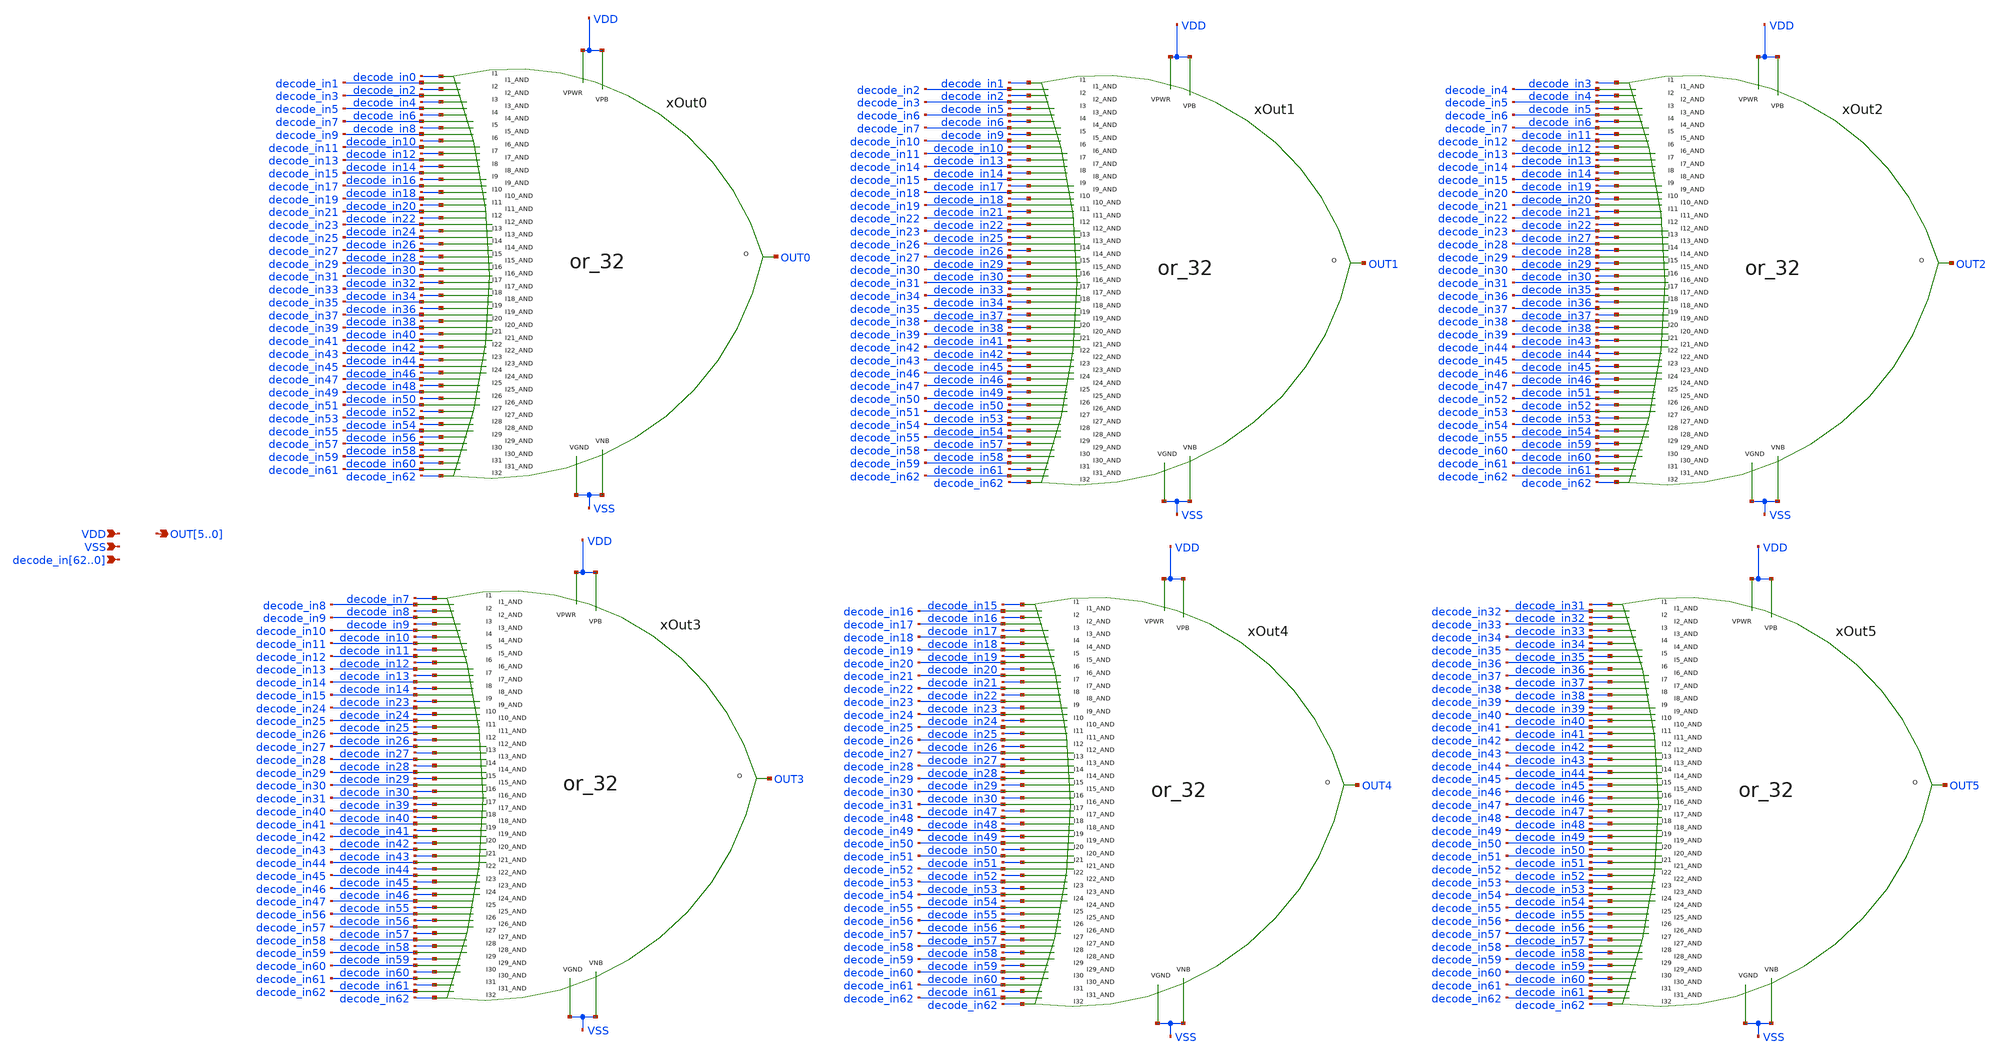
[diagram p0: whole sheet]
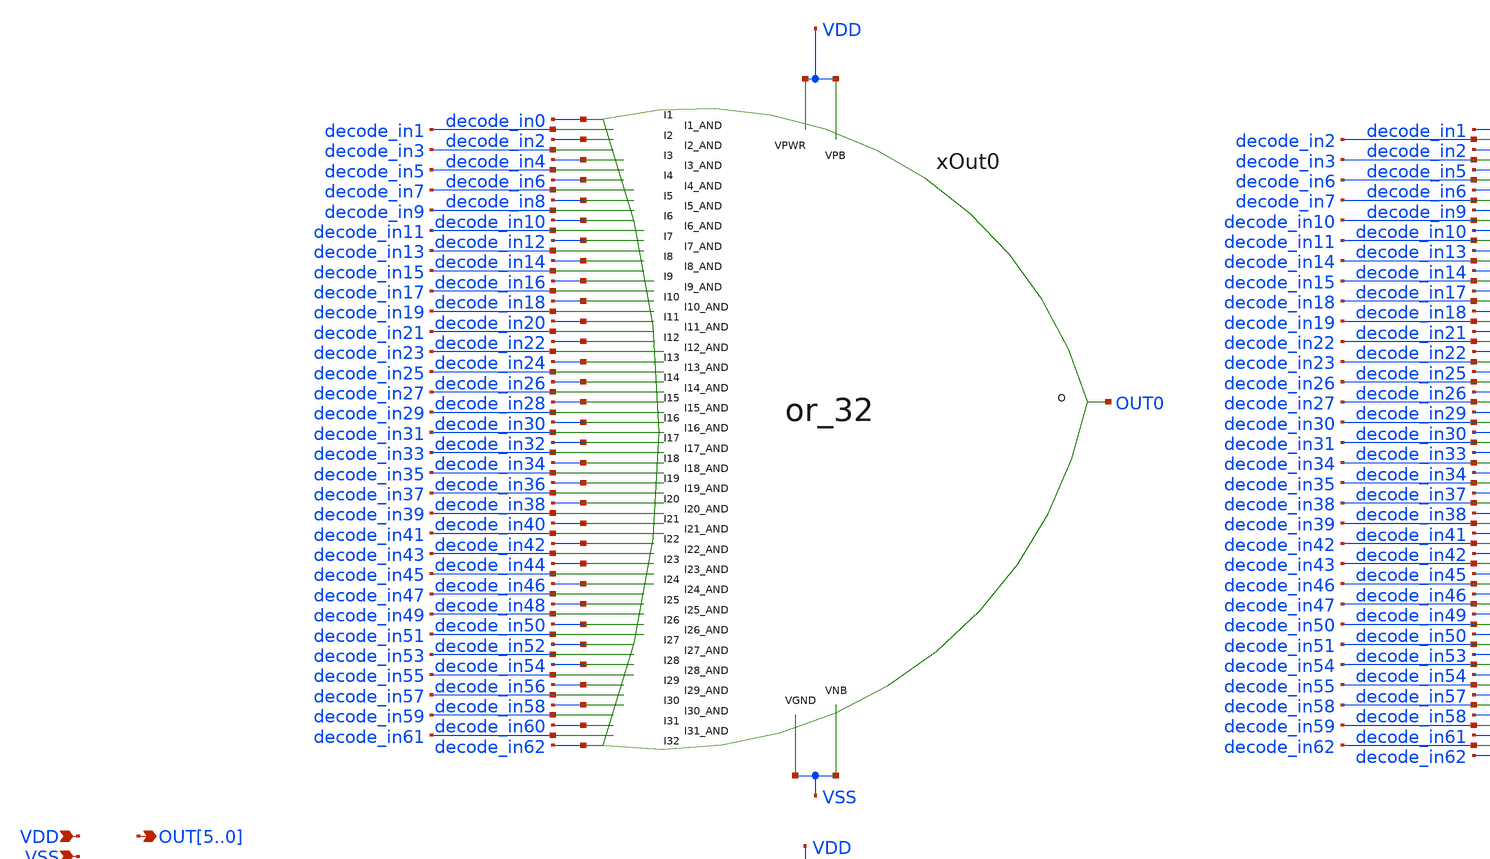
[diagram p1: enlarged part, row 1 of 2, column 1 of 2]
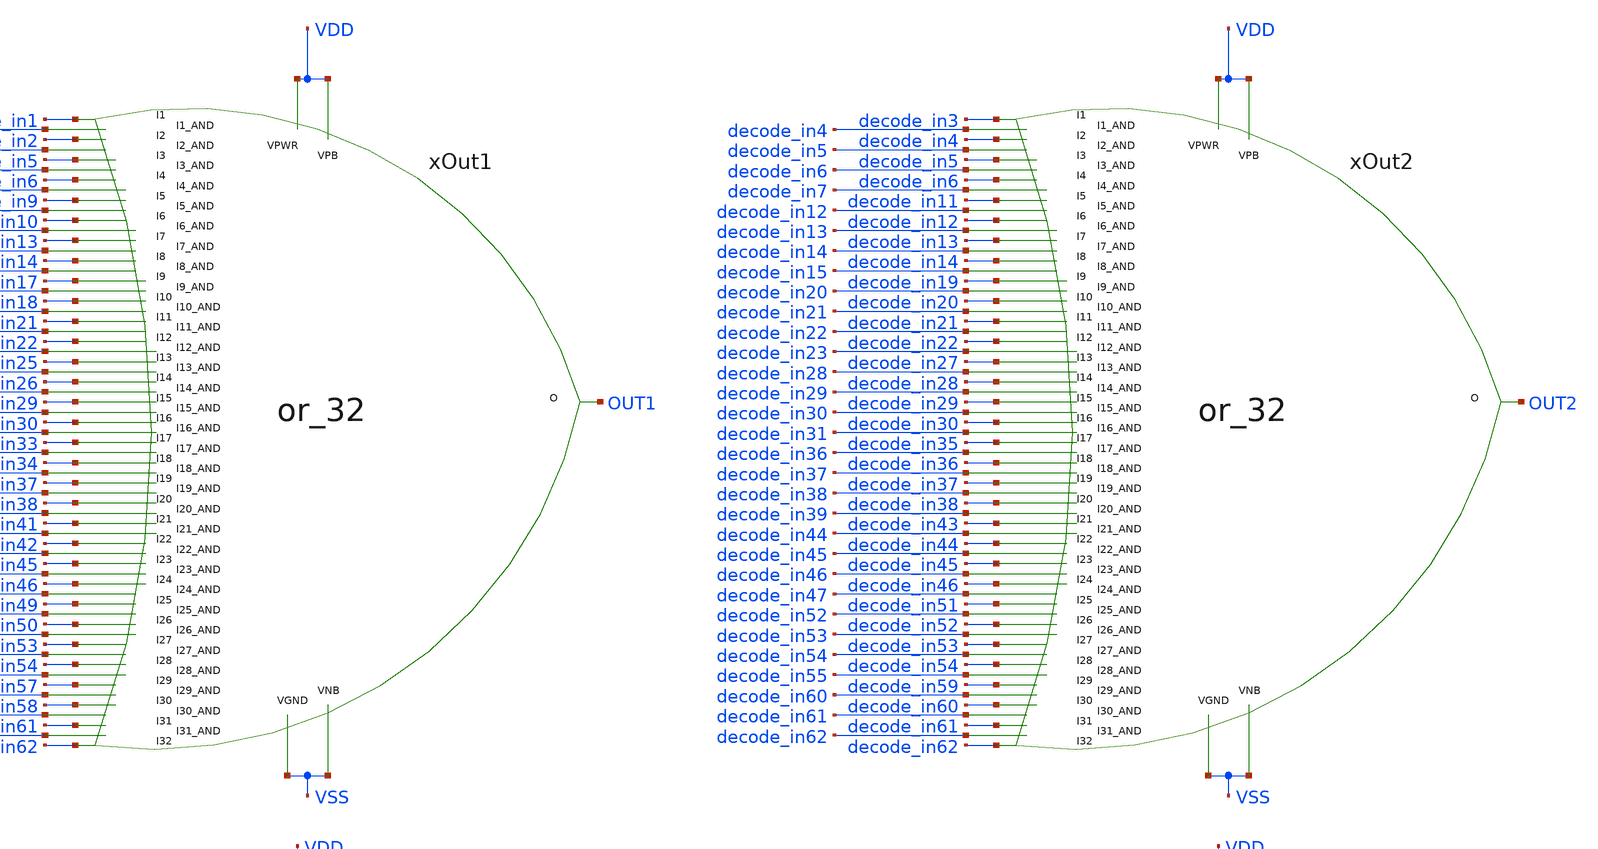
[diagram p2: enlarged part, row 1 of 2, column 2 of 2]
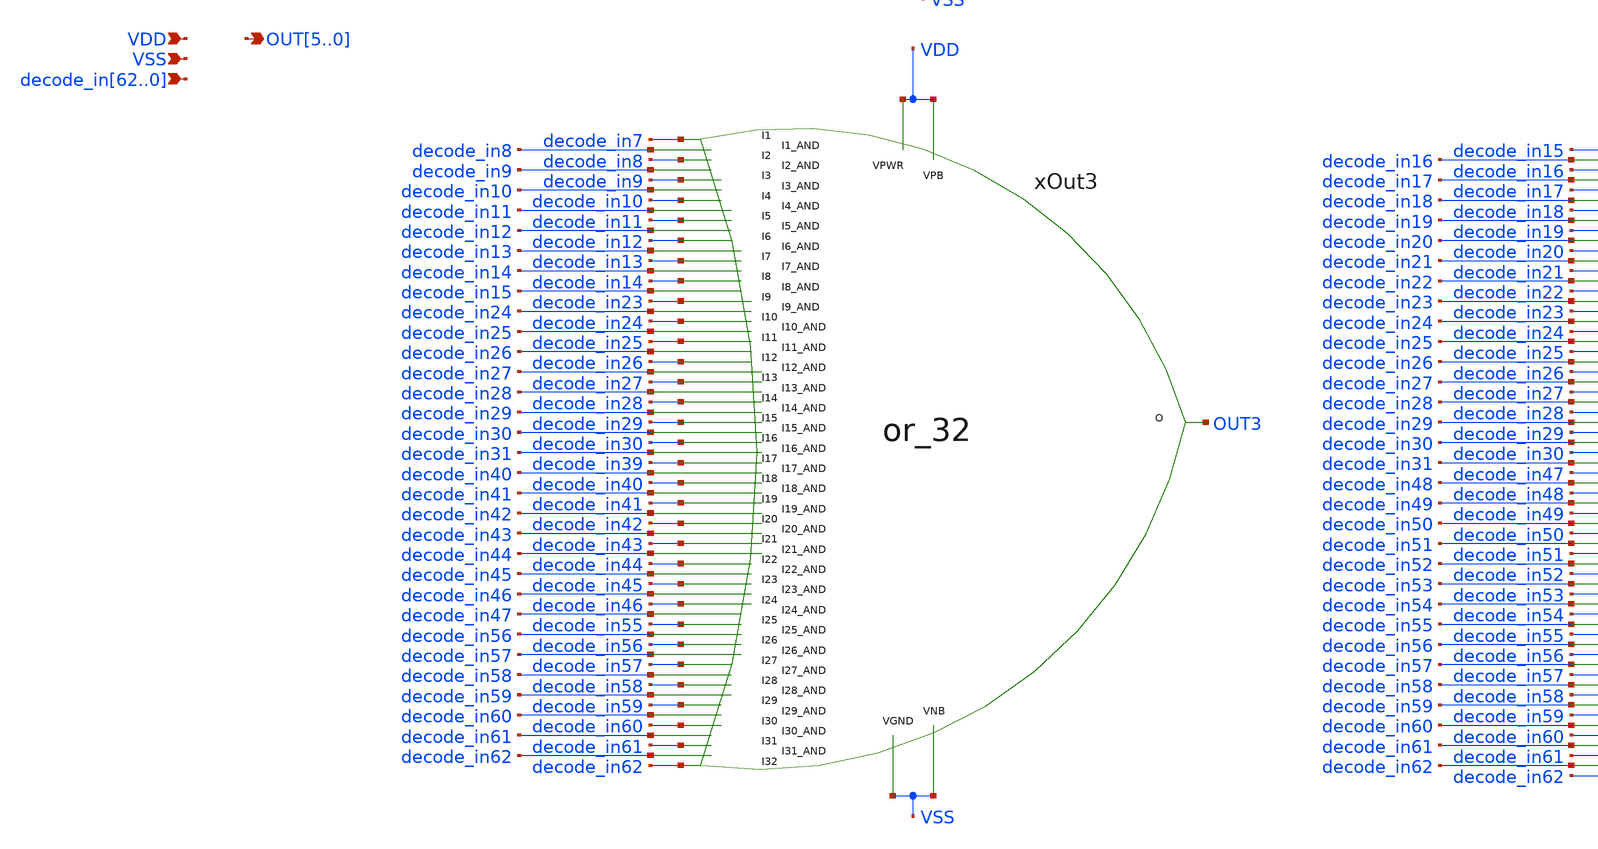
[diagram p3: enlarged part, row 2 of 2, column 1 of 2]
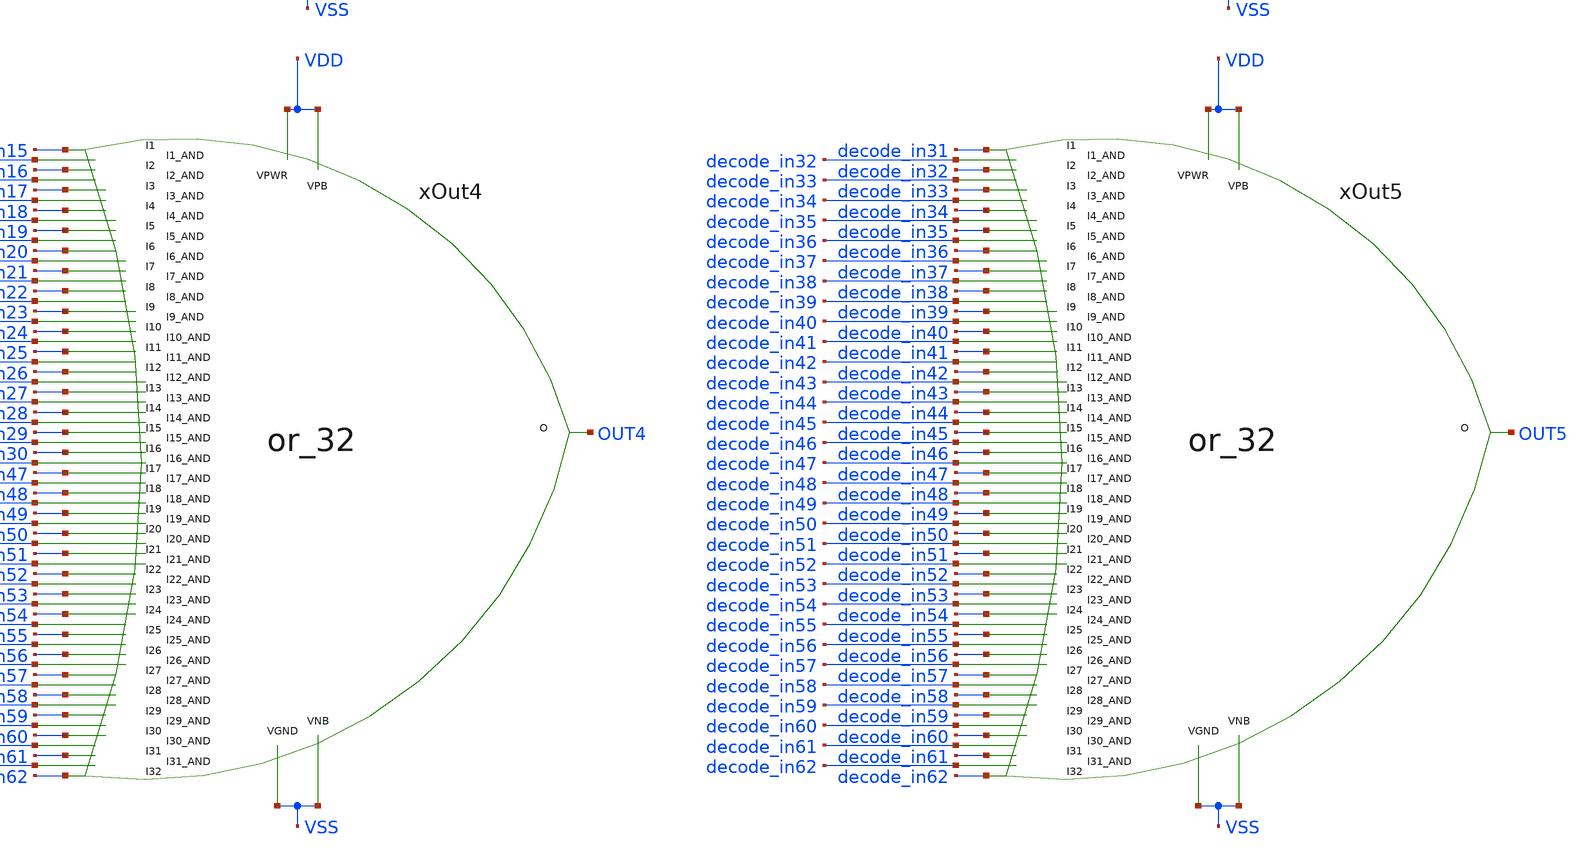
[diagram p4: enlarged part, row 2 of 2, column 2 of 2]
** sch_path: schematics/encoder_top.sch
**.subckt encoder_top
*+ decode_in62,decode_in61,decode_in60,decode_in59,decode_in58,decode_in57,decode_in56,decode_in55,decode_in54,decode_in53,decode_in52,decode_in51,decode_in50,decode_in49,decode_in48,decode_in47,decode_in46,decode_in45,decode_in44,decode_in43,decode_in42,decode_in41,decode_in40,decode_in39,decode_in38,decode_in37,decode_in36,decode_in35,decode_in34,decode_in33,decode_in32,decode_in31,decode_in30,decode_in29,decode_in28,decode_in27,decode_in26,decode_in25,decode_in24,decode_in23,decode_in22,decode_in21,decode_in20,decode_in19,decode_in18,decode_in17,decode_in16,decode_in15,decode_in14,decode_in13,decode_in12,decode_in11,decode_in10,decode_in9,decode_in8,decode_in7,decode_in6,decode_in5,decode_in4,decode_in3,decode_in2,decode_in1,decode_in0 VDD VSS OUT5,OUT4,OUT3,OUT2,OUT1,OUT0
*.ipin
*+ decode_in62,decode_in61,decode_in60,decode_in59,decode_in58,decode_in57,decode_in56,decode_in55,decode_in54,decode_in53,decode_in52,decode_in51,decode_in50,decode_in49,decode_in48,decode_in47,decode_in46,decode_in45,decode_in44,decode_in43,decode_in42,decode_in41,decode_in40,decode_in39,decode_in38,decode_in37,decode_in36,decode_in35,decode_in34,decode_in33,decode_in32,decode_in31,decode_in30,decode_in29,decode_in28,decode_in27,decode_in26,decode_in25,decode_in24,decode_in23,decode_in22,decode_in21,decode_in20,decode_in19,decode_in18,decode_in17,decode_in16,decode_in15,decode_in14,decode_in13,decode_in12,decode_in11,decode_in10,decode_in9,decode_in8,decode_in7,decode_in6,decode_in5,decode_in4,decode_in3,decode_in2,decode_in1,decode_in0
*.ipin VDD
*.ipin VSS
*.opin OUT5,OUT4,OUT3,OUT2,OUT1,OUT0
xOut0 decode_in0 decode_in2 decode_in4 decode_in6 decode_in8 decode_in10 decode_in12 decode_in14
+ decode_in16 decode_in18 decode_in20 decode_in22 decode_in24 decode_in26 decode_in28 decode_in30 decode_in32
+ decode_in34 decode_in36 decode_in38 decode_in40 decode_in42 decode_in44 decode_in46 decode_in48 decode_in50
+ decode_in52 decode_in54 decode_in56 decode_in58 decode_in60 decode_in62 OUT0 VDD VDD VSS VSS decode_in1
+ decode_in3 decode_in5 decode_in7 decode_in9 decode_in11 decode_in13 decode_in15 decode_in17 decode_in19
+ decode_in21 decode_in23 decode_in25 decode_in27 decode_in29 decode_in31 decode_in33 decode_in35 decode_in37
+ decode_in39 decode_in41 decode_in43 decode_in45 decode_in47 decode_in49 decode_in51 decode_in53 decode_in55
+ decode_in57 decode_in59 decode_in61 or_32
xOut1 decode_in1 decode_in2 decode_in5 decode_in6 decode_in9 decode_in10 decode_in13 decode_in14
+ decode_in17 decode_in18 decode_in21 decode_in22 decode_in25 decode_in26 decode_in29 decode_in30 decode_in33
+ decode_in34 decode_in37 decode_in38 decode_in41 decode_in42 decode_in45 decode_in46 decode_in49 decode_in50
+ decode_in53 decode_in54 decode_in57 decode_in58 decode_in61 decode_in62 OUT1 VDD VDD VSS VSS decode_in2
+ decode_in3 decode_in6 decode_in7 decode_in10 decode_in11 decode_in14 decode_in15 decode_in18 decode_in19
+ decode_in22 decode_in23 decode_in26 decode_in27 decode_in30 decode_in31 decode_in34 decode_in35 decode_in38
+ decode_in39 decode_in42 decode_in43 decode_in46 decode_in47 decode_in50 decode_in51 decode_in54 decode_in55
+ decode_in58 decode_in59 decode_in62 or_32
xOut2 decode_in3 decode_in4 decode_in5 decode_in6 decode_in11 decode_in12 decode_in13 decode_in14
+ decode_in19 decode_in20 decode_in21 decode_in22 decode_in27 decode_in28 decode_in29 decode_in30 decode_in35
+ decode_in36 decode_in37 decode_in38 decode_in43 decode_in44 decode_in45 decode_in46 decode_in51 decode_in52
+ decode_in53 decode_in54 decode_in59 decode_in60 decode_in61 decode_in62 OUT2 VDD VDD VSS VSS decode_in4
+ decode_in5 decode_in6 decode_in7 decode_in12 decode_in13 decode_in14 decode_in15 decode_in20 decode_in21
+ decode_in22 decode_in23 decode_in28 decode_in29 decode_in30 decode_in31 decode_in36 decode_in37 decode_in38
+ decode_in39 decode_in44 decode_in45 decode_in46 decode_in47 decode_in52 decode_in53 decode_in54 decode_in55
+ decode_in60 decode_in61 decode_in62 or_32
xOut3 decode_in7 decode_in8 decode_in9 decode_in10 decode_in11 decode_in12 decode_in13 decode_in14
+ decode_in23 decode_in24 decode_in25 decode_in26 decode_in27 decode_in28 decode_in29 decode_in30 decode_in39
+ decode_in40 decode_in41 decode_in42 decode_in43 decode_in44 decode_in45 decode_in46 decode_in55 decode_in56
+ decode_in57 decode_in58 decode_in59 decode_in60 decode_in61 decode_in62 OUT3 VDD VDD VSS VSS decode_in8
+ decode_in9 decode_in10 decode_in11 decode_in12 decode_in13 decode_in14 decode_in15 decode_in24 decode_in25
+ decode_in26 decode_in27 decode_in28 decode_in29 decode_in30 decode_in31 decode_in40 decode_in41 decode_in42
+ decode_in43 decode_in44 decode_in45 decode_in46 decode_in47 decode_in56 decode_in57 decode_in58 decode_in59
+ decode_in60 decode_in61 decode_in62 or_32
xOut4 decode_in15 decode_in16 decode_in17 decode_in18 decode_in19 decode_in20 decode_in21
+ decode_in22 decode_in23 decode_in24 decode_in25 decode_in26 decode_in27 decode_in28 decode_in29 decode_in30
+ decode_in47 decode_in48 decode_in49 decode_in50 decode_in51 decode_in52 decode_in53 decode_in54 decode_in55
+ decode_in56 decode_in57 decode_in58 decode_in59 decode_in60 decode_in61 decode_in62 OUT4 VDD VDD VSS VSS
+ decode_in16 decode_in17 decode_in18 decode_in19 decode_in20 decode_in21 decode_in22 decode_in23 decode_in24
+ decode_in25 decode_in26 decode_in27 decode_in28 decode_in29 decode_in30 decode_in31 decode_in48 decode_in49
+ decode_in50 decode_in51 decode_in52 decode_in53 decode_in54 decode_in55 decode_in56 decode_in57 decode_in58
+ decode_in59 decode_in60 decode_in61 decode_in62 or_32
xOut5 decode_in31 decode_in32 decode_in33 decode_in34 decode_in35 decode_in36 decode_in37
+ decode_in38 decode_in39 decode_in40 decode_in41 decode_in42 decode_in43 decode_in44 decode_in45 decode_in46
+ decode_in47 decode_in48 decode_in49 decode_in50 decode_in51 decode_in52 decode_in53 decode_in54 decode_in55
+ decode_in56 decode_in57 decode_in58 decode_in59 decode_in60 decode_in61 decode_in62 OUT5 VDD VDD VSS VSS
+ decode_in32 decode_in33 decode_in34 decode_in35 decode_in36 decode_in37 decode_in38 decode_in39 decode_in40
+ decode_in41 decode_in42 decode_in43 decode_in44 decode_in45 decode_in46 decode_in47 decode_in48 decode_in49
+ decode_in50 decode_in51 decode_in52 decode_in53 decode_in54 decode_in55 decode_in56 decode_in57 decode_in58
+ decode_in59 decode_in60 decode_in61 decode_in62 or_32
**.ends

* expanding   symbol:  schematics/or_32.sym # of pins=68
** sym_path: schematics/or_32.sym
** sch_path: schematics/or_32.sch
.subckt or_32 I1 I2 I3 I4 I5 I6 I7 I8 I9 I10 I11 I12 I13 I14 I15 I16 I17 I18 I19 I20 I21 I22 I23 I24
+ I25 I26 I27 I28 I29 I30 I31 I32 O VPWR VPB VGND VNB I1_AND I2_AND I3_AND I4_AND I5_AND I6_AND I7_AND
+ I8_AND I9_AND I10_AND I11_AND I12_AND I13_AND I14_AND I15_AND I16_AND I17_AND I18_AND I19_AND I20_AND
+ I21_AND I22_AND I23_AND I24_AND I25_AND I26_AND I27_AND I28_AND I29_AND I30_AND I31_AND
*.ipin I1
*.ipin I2
*.ipin I12
*.ipin I3
*.ipin I4
*.ipin I5
*.ipin I6
*.ipin I7
*.ipin I8
*.ipin I9
*.ipin I10
*.ipin I11
*.ipin I13
*.ipin I14
*.ipin I15
*.ipin I16
*.ipin I17
*.ipin I18
*.ipin I19
*.ipin I20
*.ipin I21
*.ipin I22
*.ipin I23
*.ipin I24
*.ipin I25
*.ipin I26
*.ipin I27
*.ipin I28
*.ipin I29
*.ipin I30
*.ipin I31
*.ipin I32
*.opin O
*.ipin VGND
*.ipin VNB
*.ipin VPB
*.ipin VPWR
*.ipin I1_AND
*.ipin I2_AND
*.ipin I12_AND
*.ipin I3_AND
*.ipin I4_AND
*.ipin I5_AND
*.ipin I6_AND
*.ipin I7_AND
*.ipin I8_AND
*.ipin I9_AND
*.ipin I10_AND
*.ipin I11_AND
*.ipin I13_AND
*.ipin I14_AND
*.ipin I15_AND
*.ipin I16_AND
*.ipin I17_AND
*.ipin I18_AND
*.ipin I19_AND
*.ipin I20_AND
*.ipin I21_AND
*.ipin I22_AND
*.ipin I23_AND
*.ipin I24_AND
*.ipin I25_AND
*.ipin I26_AND
*.ipin I27_AND
*.ipin I28_AND
*.ipin I29_AND
*.ipin I30_AND
*.ipin I31_AND
x10 net3 net4 net5 net6 VGND VNB VPB VPWR net1 sky130_fd_sc_hd__or4_1
x9 net1 net2 VGND VNB VPB VPWR O sky130_fd_sc_hd__or2_0
x1 I1 I1_AND I2 I2_AND I3 I3_AND I4 I4_AND VPWR VPB VGND VNB net3 or_4_and_2
x2 I5 I5_AND I6 I6_AND I7 I7_AND I8 I8_AND VPWR VPB VGND VNB net4 or_4_and_2
x3 I9 I9_AND I10 I10_AND I11 I11_AND I12 I12_AND VPWR VPB VGND VNB net5 or_4_and_2
x4 I13 I13_AND I14 I14_AND I15 I15_AND I16 I16_AND VPWR VPB VGND VNB net6 or_4_and_2
x5 net7 net8 net9 net10 VGND VNB VPB VPWR net2 sky130_fd_sc_hd__or4_1
x6 I17 I17_AND I18 I18_AND I19 I19_AND I20 I20_AND VPWR VPB VGND VNB net7 or_4_and_2
x7 I21 I21_AND I22 I22_AND I23 I23_AND I24 I24_AND VPWR VPB VGND VNB net8 or_4_and_2
x8 I25 I25_AND I26 I26_AND I27 I27_AND I28 I28_AND VPWR VPB VGND VNB net9 or_4_and_2
x11 I29 I29_AND I30 I30_AND I31 I31_AND I32 VGND VPWR VPB VGND VNB net10 or_4_and_2
.ends


* expanding   symbol:  schematics/or_4_and_2.sym # of pins=13
** sym_path: schematics/or_4_and_2.sym
** sch_path: schematics/or_4_and_2.sch
.subckt or_4_and_2 I1 I1_AND I2 I2_AND I3 I3_AND I4 I4_AND VPWR VPB VGND VNB O
*.opin O
*.ipin I1
*.ipin I2
*.ipin I3
*.ipin I4
*.ipin I1_AND
*.ipin I2_AND
*.ipin I3_AND
*.ipin I4_AND
*.ipin VGND
*.ipin VNB
*.ipin VPB
*.ipin VPWR
x1 net3 net1 net4 net2 VGND VNB VPB VPWR O sky130_fd_sc_hd__or4_1
x2 I2 net5 VGND VNB VPB VPWR net1 sky130_fd_sc_hd__and2_0
x3 I1 net6 VGND VNB VPB VPWR net3 sky130_fd_sc_hd__and2_0
x4 I4 net7 VGND VNB VPB VPWR net2 sky130_fd_sc_hd__and2_0
x5 I3 net8 VGND VNB VPB VPWR net4 sky130_fd_sc_hd__and2_0
x6 I2_AND VGND VNB VPB VPWR net5 sky130_fd_sc_hd__inv_1
x7 I1_AND VGND VNB VPB VPWR net6 sky130_fd_sc_hd__inv_1
x8 I3_AND VGND VNB VPB VPWR net8 sky130_fd_sc_hd__inv_1
x9 I4_AND VGND VNB VPB VPWR net7 sky130_fd_sc_hd__inv_1
.ends

.end
